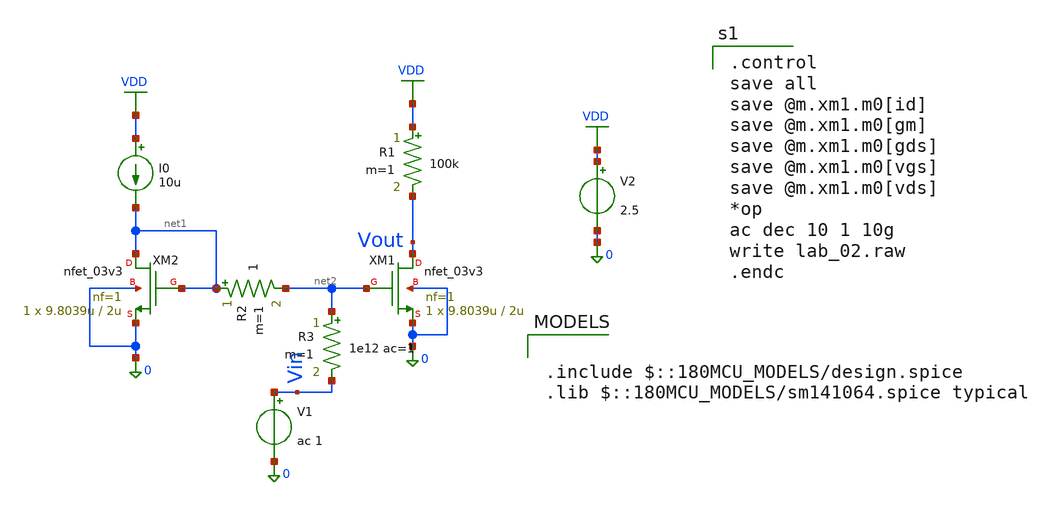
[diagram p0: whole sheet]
** sch_path: Lab_02/Lab02.sch
**.subckt Lab02
XM1 Vout net2 0 0 nfet_03v3 L=2u W=9.8039u nf=1 ad='int((nf+1)/2) * W/nf * 0.18u' as='int((nf+2)/2) * W/nf * 0.18u'
+ pd='2*int((nf+1)/2) * (W/nf + 0.18u)' ps='2*int((nf+2)/2) * (W/nf + 0.18u)' nrd='0.18u / W' nrs='0.18u / W'
+ sa=0 sb=0 sd=0 m=1
XM2 net1 net1 0 0 nfet_03v3 L=2u W=9.8039u nf=1 ad='int((nf+1)/2) * W/nf * 0.18u' as='int((nf+2)/2) * W/nf * 0.18u'
+ pd='2*int((nf+1)/2) * (W/nf + 0.18u)' ps='2*int((nf+2)/2) * (W/nf + 0.18u)' nrd='0.18u / W' nrs='0.18u / W'
+ sa=0 sb=0 sd=0 m=1
I0 VDD net1 10u
R2 net1 net2 1 m=1
V1 Vin 0 ac 1
R3 net2 Vin 1e12 ac=1 m=1
V2 VDD 0 2.5
R1 VDD Vout 100k m=1
**** begin user architecture code

.include $::180MCU_MODELS/design.spice
.lib $::180MCU_MODELS/sm141064.spice typical


.control
save all
save @m.xm1.m0[id]
save @m.xm1.m0[gm]
save @m.xm1.m0[gds]
save @m.xm1.m0[vgs]
save @m.xm1.m0[vds]
*op
ac dec 10 1 10g
write lab_02.raw
.endc

**** end user architecture code
**.ends
.GLOBAL VDD
.end
